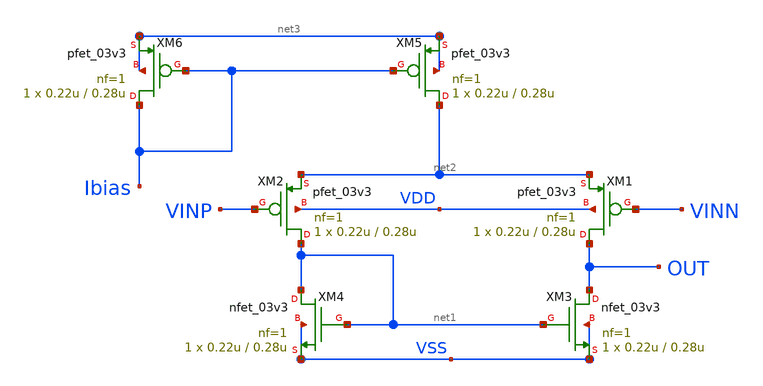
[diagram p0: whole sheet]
** sch_path: week02_current_diffpair/tugas5_cascode_current_mirror/untitled-3.sch
**.subckt untitled-3
XM1 OUT VINN net2 VDD pfet_03v3 L=0.28u W=0.22u nf=1 ad='int((nf+1)/2) * W/nf * 0.18u' as='int((nf+2)/2) * W/nf * 0.18u'
+ pd='2*int((nf+1)/2) * (W/nf + 0.18u)' ps='2*int((nf+2)/2) * (W/nf + 0.18u)' nrd='0.18u / W' nrs='0.18u / W'
+ sa=0 sb=0 sd=0 m=1
XM2 net1 VINP net2 VDD pfet_03v3 L=0.28u W=0.22u nf=1 ad='int((nf+1)/2) * W/nf * 0.18u' as='int((nf+2)/2) * W/nf * 0.18u'
+ pd='2*int((nf+1)/2) * (W/nf + 0.18u)' ps='2*int((nf+2)/2) * (W/nf + 0.18u)' nrd='0.18u / W' nrs='0.18u / W'
+ sa=0 sb=0 sd=0 m=1
XM3 OUT net1 VSS VSS nfet_03v3 L=0.28u W=0.22u nf=1 ad='int((nf+1)/2) * W/nf * 0.18u' as='int((nf+2)/2) * W/nf * 0.18u'
+ pd='2*int((nf+1)/2) * (W/nf + 0.18u)' ps='2*int((nf+2)/2) * (W/nf + 0.18u)' nrd='0.18u / W' nrs='0.18u / W'
+ sa=0 sb=0 sd=0 m=1
XM4 net1 net1 VSS VSS nfet_03v3 L=0.28u W=0.22u nf=1 ad='int((nf+1)/2) * W/nf * 0.18u' as='int((nf+2)/2) * W/nf * 0.18u'
+ pd='2*int((nf+1)/2) * (W/nf + 0.18u)' ps='2*int((nf+2)/2) * (W/nf + 0.18u)' nrd='0.18u / W' nrs='0.18u / W'
+ sa=0 sb=0 sd=0 m=1
XM5 net2 Ibias net3 net3 pfet_03v3 L=0.28u W=0.22u nf=1 ad='int((nf+1)/2) * W/nf * 0.18u' as='int((nf+2)/2) * W/nf * 0.18u'
+ pd='2*int((nf+1)/2) * (W/nf + 0.18u)' ps='2*int((nf+2)/2) * (W/nf + 0.18u)' nrd='0.18u / W' nrs='0.18u / W'
+ sa=0 sb=0 sd=0 m=1
XM6 Ibias Ibias net3 net3 pfet_03v3 L=0.28u W=0.22u nf=1 ad='int((nf+1)/2) * W/nf * 0.18u' as='int((nf+2)/2) * W/nf * 0.18u'
+ pd='2*int((nf+1)/2) * (W/nf + 0.18u)' ps='2*int((nf+2)/2) * (W/nf + 0.18u)' nrd='0.18u / W' nrs='0.18u / W'
+ sa=0 sb=0 sd=0 m=1
**.ends
.end
